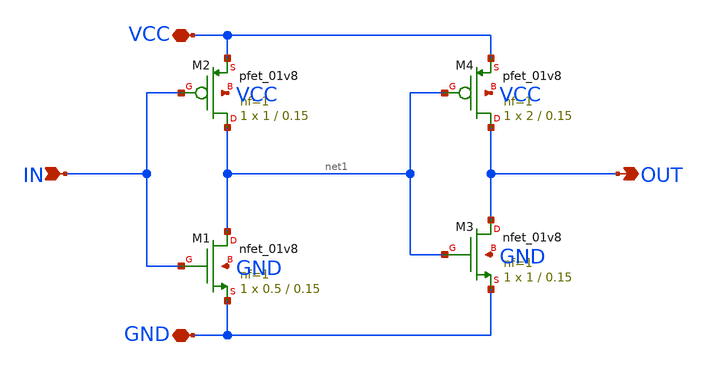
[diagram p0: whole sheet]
** sch_path: blocks/04_1Bit_DAC/xschem/BUF_B01.sch
**.subckt BUF_B01 VCC GND IN OUT
*.iopin VCC
*.iopin GND
*.ipin IN
*.opin OUT
XM1 net1 IN GND GND sky130_fd_pr__nfet_01v8 L=0.15 W=0.5 nf=1 ad='int((1 + 1)/2) * 0.5 / 1 * 0.29' as='int((1 + 2)/2) * 0.5 / 1 * 0.29'
+ pd='2*int((1 + 1)/2) * (0.5 / 1 + 0.29)' ps='2*int((1 + 2)/2) * (0.5 / 1 + 0.29)' nrd='0.29 / 0.5 ' nrs='0.29 / 0.5 '
+ sa=0 sb=0 sd=0 mult=1 m=1
XM2 net1 IN VCC VCC sky130_fd_pr__pfet_01v8 L=0.15 W=1 nf=1 ad='int((1 + 1)/2) * 1 / 1 * 0.29' as='int((1 + 2)/2) * 1 / 1 * 0.29'
+ pd='2*int((1 + 1)/2) * (1 / 1 + 0.29)' ps='2*int((1 + 2)/2) * (1 / 1 + 0.29)' nrd='0.29 / 1 ' nrs='0.29 / 1 '
+ sa=0 sb=0 sd=0 mult=1 m=1
XM3 OUT net1 GND GND sky130_fd_pr__nfet_01v8 L=0.15 W=1 nf=1 ad='int((1 + 1)/2) * 1 / 1 * 0.29' as='int((1 + 2)/2) * 1 / 1 * 0.29'
+ pd='2*int((1 + 1)/2) * (1 / 1 + 0.29)' ps='2*int((1 + 2)/2) * (1 / 1 + 0.29)' nrd='0.29 / 1 ' nrs='0.29 / 1 '
+ sa=0 sb=0 sd=0 mult=1 m=1
XM4 OUT net1 VCC VCC sky130_fd_pr__pfet_01v8 L=0.15 W=2 nf=1 ad='int((1 + 1)/2) * 2 / 1 * 0.29' as='int((1 + 2)/2) * 2 / 1 * 0.29'
+ pd='2*int((1 + 1)/2) * (2 / 1 + 0.29)' ps='2*int((1 + 2)/2) * (2 / 1 + 0.29)' nrd='0.29 / 2 ' nrs='0.29 / 2 '
+ sa=0 sb=0 sd=0 mult=1 m=1
**.ends
.end
